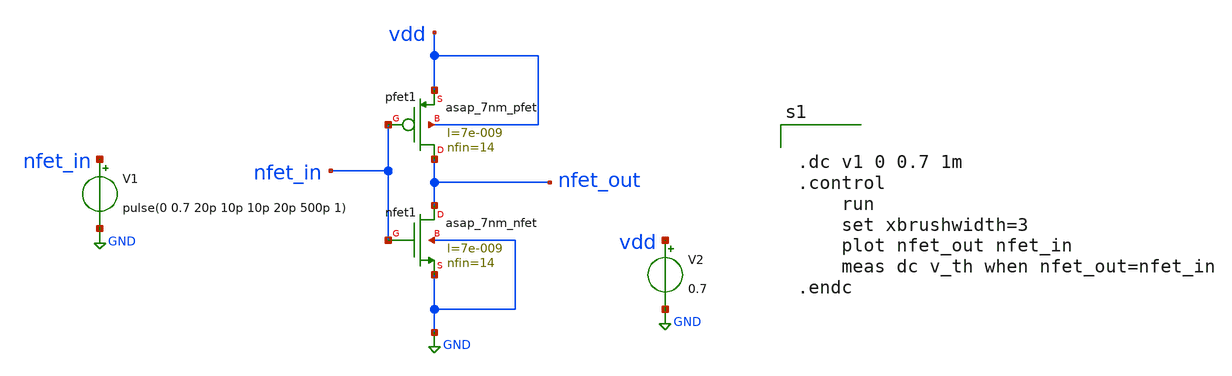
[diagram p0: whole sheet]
** sch_path: Module2/Spice files/inverter_vtc.sch
**.subckt inverter_vtc
V1 nfet_in GND pulse(0 0.7 20p 10p 10p 20p 500p 1)
V2 vdd GND 0.7
Xpfet1 nfet_out nfet_in vdd vdd asap_7nm_pfet l=7e-009 nfin=14
Xnfet1 nfet_out nfet_in GND GND asap_7nm_nfet l=7e-009 nfin=14
**** begin user architecture code


.dc v1 0 0.7 1m
.control
    run
    set xbrushwidth=3
    plot nfet_out nfet_in
    meas dc v_th when nfet_out=nfet_in
.endc


**** end user architecture code
**.ends
.GLOBAL GND
.end
